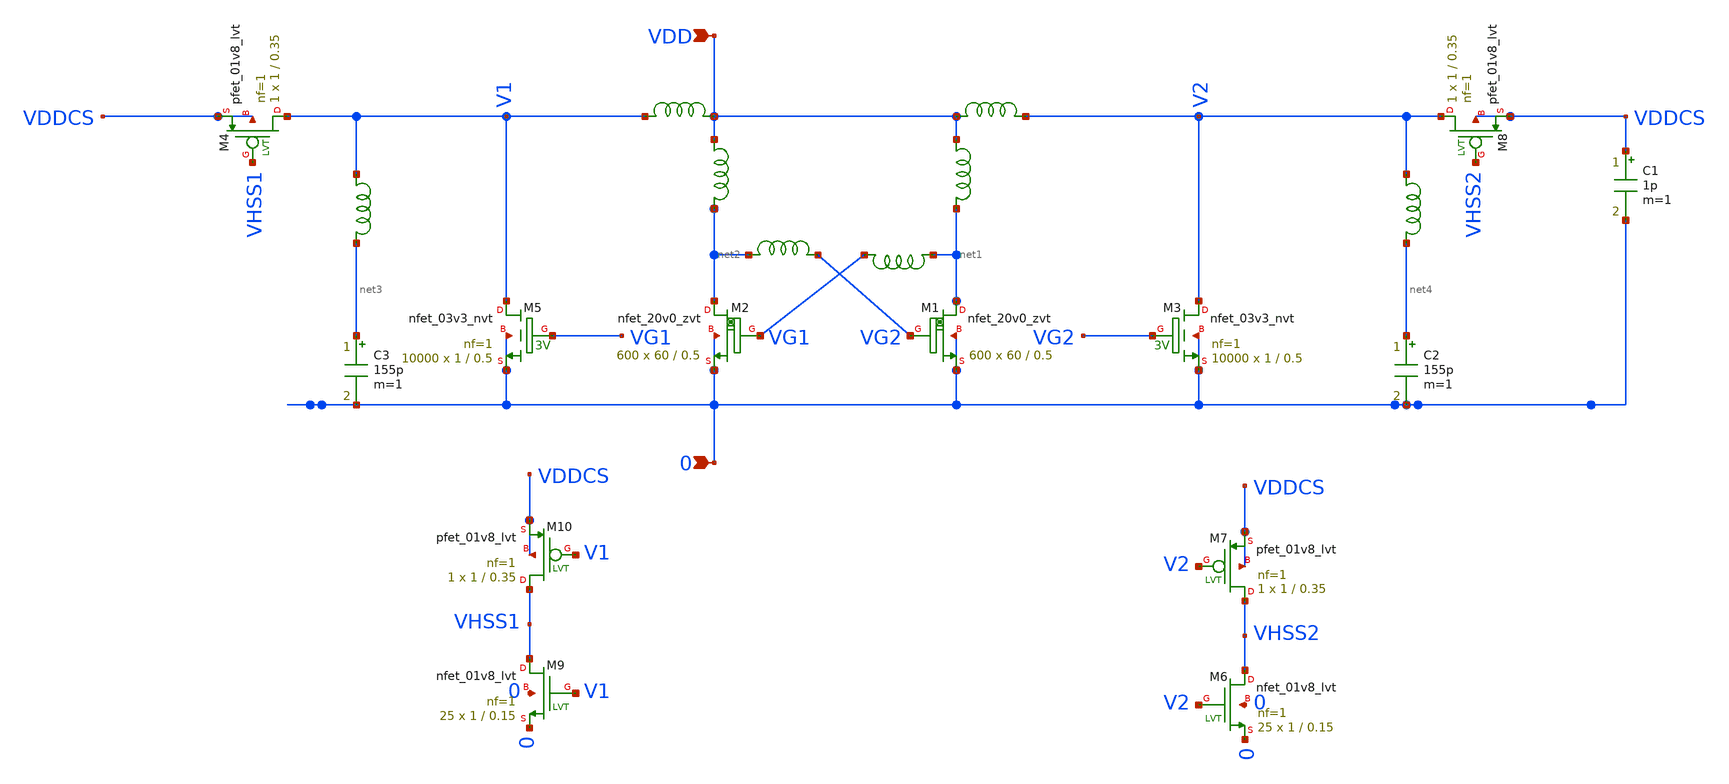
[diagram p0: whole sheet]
** sch_path: design/LELO_SVOD_SKY130A/LELO_EXSC.sch
**.subckt LELO_EXSC 0 VDD
*.ipin 0
*.ipin VDD
x3 VDD net1 1812PS-102_imp
x4 VDD net2 1812PS-102_imp
XM1 net1 VG2 0 0 sky130_fd_pr__nfet_20v0_zvt W=60 L=0.5 m=600
XM2 net2 VG1 0 0 sky130_fd_pr__nfet_20v0_zvt W=60 L=0.5 m=600
x1 net2 VG2 1812PS-104_imp
x2 net1 VG1 1812PS-104_imp
C1 VDDCS 0 1p m=1
XM4 V1 VHSS1 VDDCS VDDCS sky130_fd_pr__pfet_01v8_lvt L=0.35 W=1 nf=1 ad='int((1 + 1)/2) * 1 / 1 * 0.29'
+ as='int((1 + 2)/2) * 1 / 1 * 0.29' pd='2*int((1 + 1)/2) * (1 / 1 + 0.29)' ps='2*int((1 + 2)/2) * (1 / 1 + 0.29)'
+ nrd='0.29 / 1 ' nrs='0.29 / 1 ' sa=0 sb=0 sd=0 mult=1 m=1
XM8 V2 VHSS2 VDDCS VDDCS sky130_fd_pr__pfet_01v8_lvt L=0.35 W=1 nf=1 ad='int((1 + 1)/2) * 1 / 1 * 0.29'
+ as='int((1 + 2)/2) * 1 / 1 * 0.29' pd='2*int((1 + 1)/2) * (1 / 1 + 0.29)' ps='2*int((1 + 2)/2) * (1 / 1 + 0.29)'
+ nrd='0.29 / 1 ' nrs='0.29 / 1 ' sa=0 sb=0 sd=0 mult=1 m=1
XM6 VHSS2 V2 0 0 sky130_fd_pr__nfet_01v8_lvt L=0.15 W=1 nf=1 ad='int((1 + 1)/2) * 1 / 1 * 0.29' as='int((1 + 2)/2) * 1 / 1 * 0.29'
+ pd='2*int((1 + 1)/2) * (1 / 1 + 0.29)' ps='2*int((1 + 2)/2) * (1 / 1 + 0.29)' nrd='0.29 / 1 ' nrs='0.29 / 1 '
+ sa=0 sb=0 sd=0 mult=25 m=25
XM9 VHSS1 V1 0 0 sky130_fd_pr__nfet_01v8_lvt L=0.15 W=1 nf=1 ad='int((1 + 1)/2) * 1 / 1 * 0.29' as='int((1 + 2)/2) * 1 / 1 * 0.29'
+ pd='2*int((1 + 1)/2) * (1 / 1 + 0.29)' ps='2*int((1 + 2)/2) * (1 / 1 + 0.29)' nrd='0.29 / 1 ' nrs='0.29 / 1 '
+ sa=0 sb=0 sd=0 mult=25 m=25
XM3 V2 VG2 0 0 sky130_fd_pr__nfet_03v3_nvt L=0.5 W=1 nf=1 ad='int((1 + 1)/2) * 1 / 1 * 0.29' as='int((1 + 2)/2) * 1 / 1 * 0.29'
+ pd='2*int((1 + 1)/2) * (1 / 1 + 0.29)' ps='2*int((1 + 2)/2) * (1 / 1 + 0.29)' nrd='0.29 / 1 ' nrs='0.29 / 1 '
+ sa=0 sb=0 sd=0 mult=10000 m=10000
XM5 V1 VG1 0 0 sky130_fd_pr__nfet_03v3_nvt L=0.5 W=1 nf=1 ad='int((1 + 1)/2) * 1 / 1 * 0.29' as='int((1 + 2)/2) * 1 / 1 * 0.29'
+ pd='2*int((1 + 1)/2) * (1 / 1 + 0.29)' ps='2*int((1 + 2)/2) * (1 / 1 + 0.29)' nrd='0.29 / 1 ' nrs='0.29 / 1 '
+ sa=0 sb=0 sd=0 mult=10000 m=10000
x6 VDD V2 1812PS-684_imp
x5 V1 VDD 1812PS-684_imp
C3 net3 0 155p m=1
x8 V1 net3 1812PS-334_imp
C2 net4 0 155p m=1
x7 V2 net4 1812PS-334_imp
XM7 VHSS2 V2 VDDCS VDDCS sky130_fd_pr__pfet_01v8_lvt L=0.35 W=1 nf=1 ad='int((1 + 1)/2) * 1 / 1 * 0.29'
+ as='int((1 + 2)/2) * 1 / 1 * 0.29' pd='2*int((1 + 1)/2) * (1 / 1 + 0.29)' ps='2*int((1 + 2)/2) * (1 / 1 + 0.29)'
+ nrd='0.29 / 1 ' nrs='0.29 / 1 ' sa=0 sb=0 sd=0 mult=1 m=1
XM10 VHSS1 V1 VDDCS VDDCS sky130_fd_pr__pfet_01v8_lvt L=0.35 W=1 nf=1 ad='int((1 + 1)/2) * 1 / 1 * 0.29'
+ as='int((1 + 2)/2) * 1 / 1 * 0.29' pd='2*int((1 + 1)/2) * (1 / 1 + 0.29)' ps='2*int((1 + 2)/2) * (1 / 1 + 0.29)'
+ nrd='0.29 / 1 ' nrs='0.29 / 1 ' sa=0 sb=0 sd=0 mult=1 m=1
**.ends

* expanding   symbol:  LELO_SVOD_SKY130A/1812PS-102_imp.sym # of pins=2
** sym_path: design/LELO_SVOD_SKY130A/1812PS-102_imp.sym

.subckt 1812PS-102_imp port1 port2
X1 port1 port2 Model1D R1=60 R2=0.054 C= 0.15p K1=0.000001 K2=0.064 K3= 1u K4=1E-06 K5=0.000001 L=0
+ Is=0 a=0 L_Z0=0 L_EL=0 L_F0=0E6 PkZ=1282.46492
.ends 1812PS-102_imp

* expanding   symbol:  LELO_SVOD_SKY130A/1812PS-104_imp.sym # of pins=2
** sym_path: design/LELO_SVOD_SKY130A/1812PS-104_imp.sym

.subckt 1812PS-104_imp port1 port2
X1 port1 port2 Model1D R1=40 R2=1.3 C= 1.6p K1=0.000001 K2=13.98 K3= 100u K4=0.000001 K5=0.000001
+ L=0 Is=0 a=0 L_Z0=0 L_EL=0 L_F0=0E6 PkZ=48065.0165
.ends 1812PS-104_imp

* expanding   symbol:  LELO_SVOD_SKY130A/1812PS-684_imp.sym # of pins=2
** sym_path: design/LELO_SVOD_SKY130A/1812PS-684_imp.sym

.subckt 1812PS-684_imp port1 port2
X1 port1 port2 Model1D R1=60 R2=6.6 C= 9.85p K1=0.000001 K2=152.8 K3= 680u K4=0.000001 K5=0.000001
+ L=0 Is=0 a=0 L_Z0=0 L_EL=0 L_F0=0E6 PkZ=179794.129
.ends 1812PS-684_imp

* expanding   symbol:  LELO_SVOD_SKY130A/1812PS-334_imp.sym # of pins=2
** sym_path: design/LELO_SVOD_SKY130A/1812PS-334_imp.sym

.subckt 1812PS-334_imp port1 port2
X1 port1 port2 Model1D R1=75 R2=4.9 C= 2.43p K1=1E-06 K2=57.9 K3= 330u K4=0.000001 K5=0.000001 L=0
+ Is=0 a=0 L_Z0=0 L_EL=0 L_F0=0E6 PkZ=127597.141
.ends 1812PS-334_imp

.end
